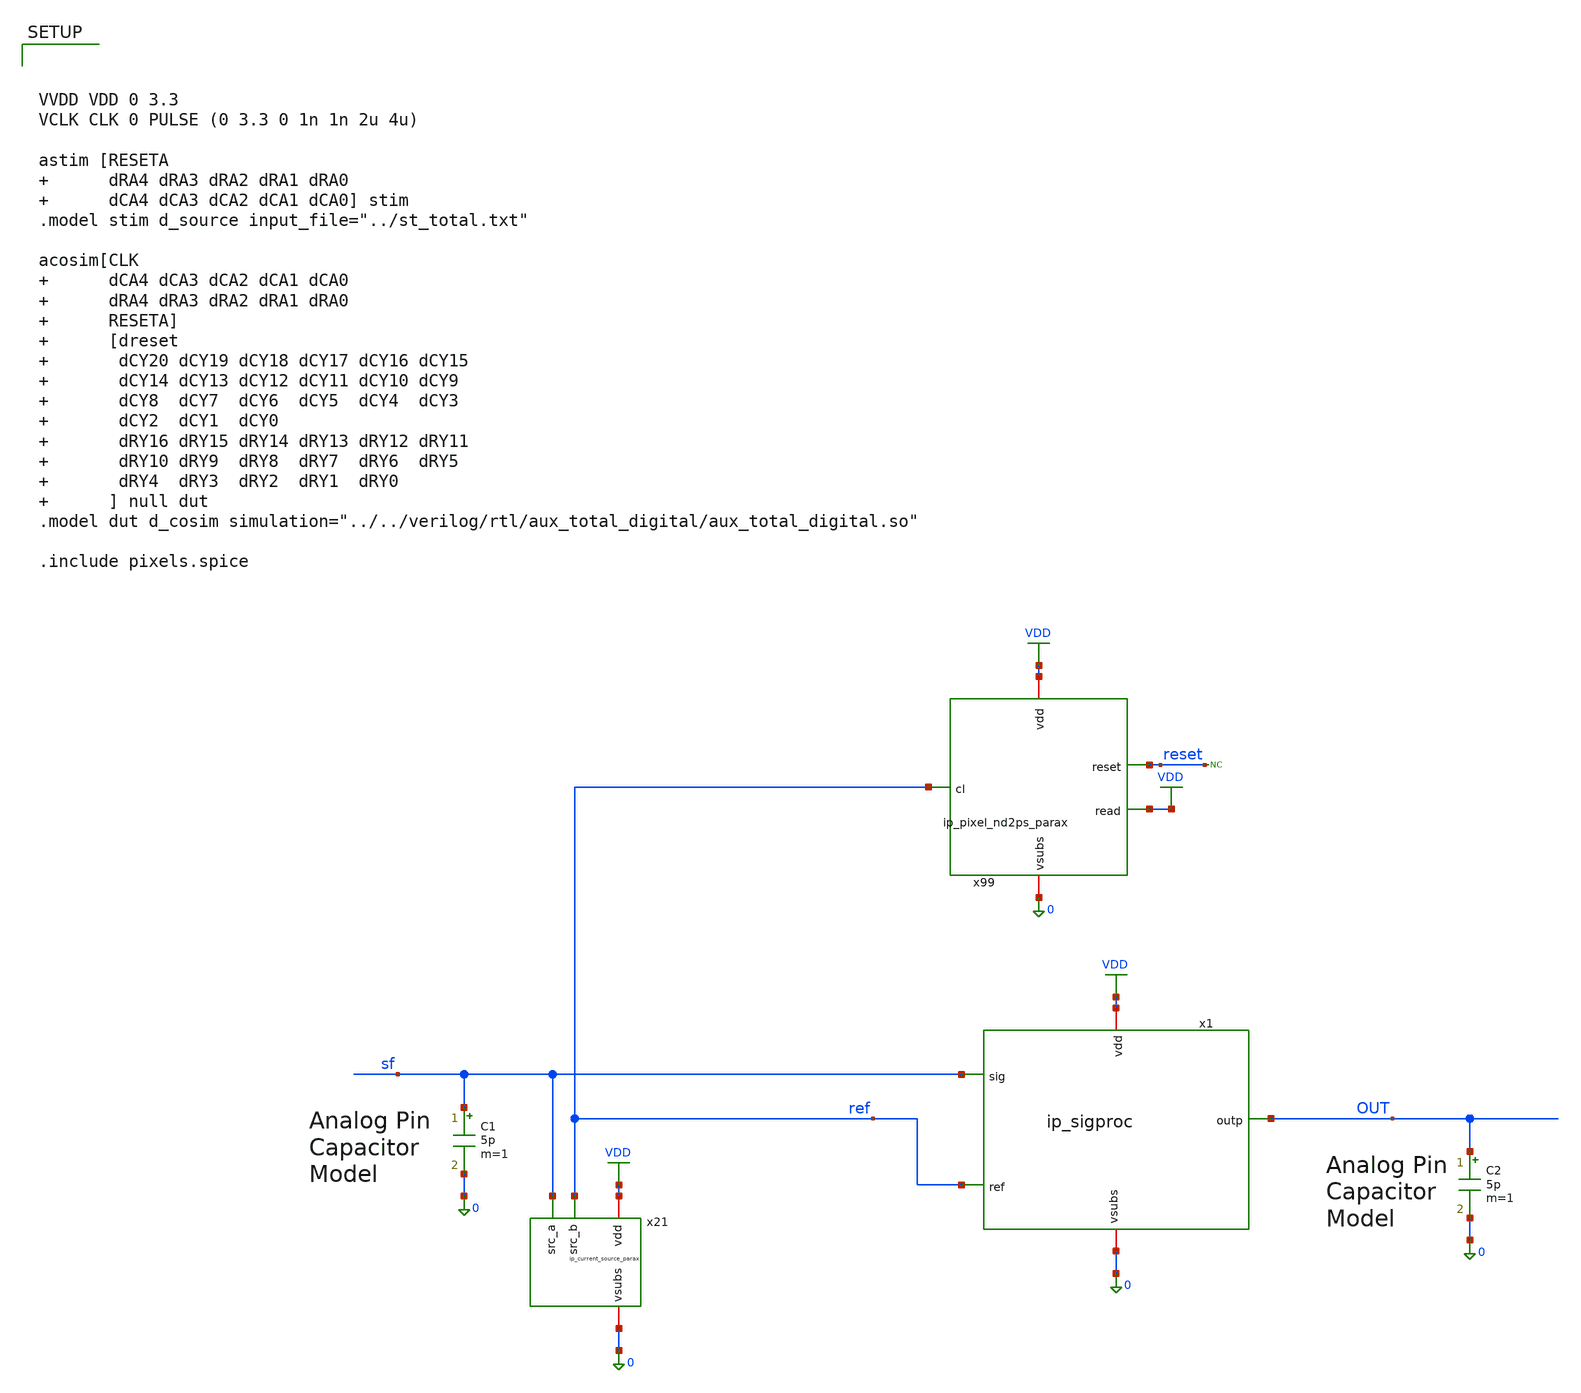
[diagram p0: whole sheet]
** sch_path: xschem/tb_total_tran.sch
**.subckt tb_total_tran
x21 VDD sf 0 ref ip_current_source_parax
x99 VDD reset VDD 0 ref ip_pixel_nd2ps_parax
C1 sf 0 5p m=1
C2 OUT 0 5p m=1
* noconn reset
x1 VDD OUT sf ref 0 ip_sigproc
**** begin user architecture code

.include $::180MCU_MODELS/design.ngspice
.lib $::180MCU_MODELS/sm141064.ngspice typical
.lib $::180MCU_MODELS/sm141064.ngspice res_typical
.lib $::180MCU_MODELS/sm141064.ngspice moscap_typical
.lib $::180MCU_MODELS/sm141064.ngspice diode_typical




.option klu
.option reltol=0.05
.option abstol=100u
.save none

.save V(nRA0) V(nRA1) V(nRA2) V(nRA3) V(nRA4)
.save V(nCA0) V(nCA1) V(nCA2) V(nCA3) V(nCA4)

.save V(ncy0) V(ncy1) V(ncy2) V(ncy3) V(ncy4) V(ncy5) V(ncy6) V(ncy7) V(ncy8)
.save V(ncy9) V(ncy10) V(ncy11) V(ncy12) V(ncy13) V(ncy14) V(ncy15) V(ncy16)
.save V(ncy17) V(ncy18) V(ncy19) V(ncy20)

.save V(nry0) V(nry1) V(nry2) V(nry3) V(nry4) V(nry5) V(nry6) V(nry7) V(nry8)
.save V(nry9) V(nry10) V(nry11) V(nry12) V(nry13) V(nry14) V(nry15) V(nry16)

.save V(reset) V(clk)
.save V(out) V(sf) V(ref) V(amp)
.control
	reset
	tran 100n 5.2m 0 100n
	write tb_total_tran.raw
	quit
.endc






VVDD VDD 0 3.3
VCLK CLK 0 PULSE (0 3.3 0 1n 1n 2u 4u)

astim [RESETA        dRA4 dRA3 dRA2 dRA1 dRA0        dCA4 dCA3 dCA2 dCA1 dCA0] stim
.model stim d_source input_file="../st_total.txt"

acosim[CLK        dCA4 dCA3 dCA2 dCA1 dCA0        dRA4 dRA3 dRA2 dRA1 dRA0        RESETA]
+        [dreset        dCY20 dCY19 dCY18 dCY17 dCY16 dCY15        dCY14 dCY13 dCY12 dCY11 dCY10 dCY9         dCY8
+  dCY7  dCY6  dCY5  dCY4  dCY3         dCY2  dCY1  dCY0         dRY16 dRY15 dRY14 dRY13 dRY12 dRY11
+         dRY10 dRY9  dRY8  dRY7  dRY6  dRY5        dRY4  dRY3  dRY2  dRY1  dRY0        ] null dut
.model dut d_cosim simulation="../../verilog/rtl/aux_total_digital/aux_total_digital.so"

.include pixels.spice


**** end user architecture code
**.ends

* expanding   symbol:  ip_current_source_parax.sym # of pins=4
** sym_path: xschem/ip_current_source.sym
.include [file normalize ./parax/ip_current_source.sim.spice]

* expanding   symbol:  ip_pixel_nd2ps_parax.sym # of pins=5
** sym_path: xschem/ip_pixel_nd2ps.sym
.include [file normalize ./parax/ip_pixel_nd2ps.sim.spice]

* expanding   symbol:  ip_sigproc.sym # of pins=5
** sym_path: xschem/ip_sigproc.sym
** sch_path: xschem/ip_sigproc.sch
.subckt ip_sigproc vdd outp sig ref vsubs
*.ipin sig
*.ipin ref
*.iopin vdd
*.iopin vsubs
*.opin outp
x1 vdd net1 sig net1 vsubs ip_amplifier
x2 vdd outp ref net2 net6 ip_amplifier
XR1 net1 net2 net7 ppolyf_u_1k r_width=1e-6 r_length=10e-6 m=1
XR2 net2 net3 net8 ppolyf_u_1k r_width=1e-6 r_length=10e-6 m=1
XR3 net3 net4 net9 ppolyf_u_1k r_width=1e-6 r_length=10e-6 m=1
XR4 net4 net5 net10 ppolyf_u_1k r_width=1e-6 r_length=10e-6 m=1
XR5 net5 outp net11 ppolyf_u_1k r_width=1e-6 r_length=10e-6 m=1
XC1 outp net2 cap_pmos_03v3 c_width=12e-6 c_length=12e-6 m=1
XC2 net2 outp cap_pmos_03v3 c_width=12e-6 c_length=12e-6 m=1
.ends


* expanding   symbol:  xschem/ip_amplifier.sym # of pins=5
** sym_path: xschem/ip_amplifier.sym
** sch_path: xschem/ip_amplifier.sch
.subckt ip_amplifier VDD OUTP INP INN VSUBS
*.iopin VDD
*.iopin VSUBS
*.ipin INP
*.ipin INN
*.opin OUTP
XM1 COMP INP COMMON_ VDD pfet_03v3 L=5u W=18.0u nf=1 ad='int((nf+1)/2) * W/nf * 0.18u' as='int((nf+2)/2) * W/nf * 0.18u'
+ pd='2*int((nf+1)/2) * (W/nf + 0.18u)' ps='2*int((nf+2)/2) * (W/nf + 0.18u)' nrd='0.18u / W' nrs='0.18u / W'
+ sa=0 sb=0 sd=0 m=1 par=1
XM2 net6 INN COMMON_ VDD pfet_03v3 L=5u W=18.0u nf=1 ad='int((nf+1)/2) * W/nf * 0.18u' as='int((nf+2)/2) * W/nf * 0.18u'
+ pd='2*int((nf+1)/2) * (W/nf + 0.18u)' ps='2*int((nf+2)/2) * (W/nf + 0.18u)' nrd='0.18u / W' nrs='0.18u / W'
+ sa=0 sb=0 sd=0 m=1 par=1
XM3 net2 NBIAS VSUBS vsubs nfet_03v3 L=2u W=6u nf=1 ad='int((nf+1)/2) * W/nf * 0.18u' as='int((nf+2)/2) * W/nf * 0.18u'
+ pd='2*int((nf+1)/2) * (W/nf + 0.18u)' ps='2*int((nf+2)/2) * (W/nf + 0.18u)' nrd='0.18u / W' nrs='0.18u / W'
+ sa=0 sb=0 sd=0 m=2 par=2
XM4 net1 NBIAS VSUBS vsubs nfet_03v3 L=2u W=6u nf=1 ad='int((nf+1)/2) * W/nf * 0.18u' as='int((nf+2)/2) * W/nf * 0.18u'
+ pd='2*int((nf+1)/2) * (W/nf + 0.18u)' ps='2*int((nf+2)/2) * (W/nf + 0.18u)' nrd='0.18u / W' nrs='0.18u / W'
+ sa=0 sb=0 sd=0 m=1 par=1
XM7 NBIAS NBIAS net2 vsubs nfet_03v3 L=0.5u W=6u nf=1 ad='int((nf+1)/2) * W/nf * 0.18u' as='int((nf+2)/2) * W/nf * 0.18u'
+ pd='2*int((nf+1)/2) * (W/nf + 0.18u)' ps='2*int((nf+2)/2) * (W/nf + 0.18u)' nrd='0.18u / W' nrs='0.18u / W'
+ sa=0 sb=0 sd=0 m=4 par=4
XM8 net3 NBIAS net1 vsubs nfet_03v3 L=0.5u W=6u nf=1 ad='int((nf+1)/2) * W/nf * 0.18u' as='int((nf+2)/2) * W/nf * 0.18u'
+ pd='2*int((nf+1)/2) * (W/nf + 0.18u)' ps='2*int((nf+2)/2) * (W/nf + 0.18u)' nrd='0.18u / W' nrs='0.18u / W'
+ sa=0 sb=0 sd=0 m=4 par=4
XM9 net4 PBIAS VDD VDD pfet_03v3 L=2u W=6u nf=1 ad='int((nf+1)/2) * W/nf * 0.18u' as='int((nf+2)/2) * W/nf * 0.18u'
+ pd='2*int((nf+1)/2) * (W/nf + 0.18u)' ps='2*int((nf+2)/2) * (W/nf + 0.18u)' nrd='0.18u / W' nrs='0.18u / W'
+ sa=0 sb=0 sd=0 m=1 par=1
XM10 net5 PBIAS VDD VDD pfet_03v3 L=2u W=6u nf=1 ad='int((nf+1)/2) * W/nf * 0.18u' as='int((nf+2)/2) * W/nf * 0.18u'
+ pd='2*int((nf+1)/2) * (W/nf + 0.18u)' ps='2*int((nf+2)/2) * (W/nf + 0.18u)' nrd='0.18u / W' nrs='0.18u / W'
+ sa=0 sb=0 sd=0 m=1 par=1
XM11 PBIAS PBIAS net4 VDD pfet_03v3 L=0.5u W=6u nf=1 ad='int((nf+1)/2) * W/nf * 0.18u' as='int((nf+2)/2) * W/nf * 0.18u'
+ pd='2*int((nf+1)/2) * (W/nf + 0.18u)' ps='2*int((nf+2)/2) * (W/nf + 0.18u)' nrd='0.18u / W' nrs='0.18u / W'
+ sa=0 sb=0 sd=0 m=4 par=4
XM12 COMMON PBIAS net5 VDD pfet_03v3 L=0.5u W=6u nf=1 ad='int((nf+1)/2) * W/nf * 0.18u' as='int((nf+2)/2) * W/nf * 0.18u'
+ pd='2*int((nf+1)/2) * (W/nf + 0.18u)' ps='2*int((nf+2)/2) * (W/nf + 0.18u)' nrd='0.18u / W' nrs='0.18u / W'
+ sa=0 sb=0 sd=0 m=4 par=4
XM13 COMP net6 VSUBS vsubs nfet_03v3 L=5u W=6u nf=1 ad='int((nf+1)/2) * W/nf * 0.18u' as='int((nf+2)/2) * W/nf * 0.18u'
+ pd='2*int((nf+1)/2) * (W/nf + 0.18u)' ps='2*int((nf+2)/2) * (W/nf + 0.18u)' nrd='0.18u / W' nrs='0.18u / W'
+ sa=0 sb=0 sd=0 m=1 par=1
XM14 net6 net6 VSUBS vsubs nfet_03v3 L=5u W=6u nf=1 ad='int((nf+1)/2) * W/nf * 0.18u' as='int((nf+2)/2) * W/nf * 0.18u'
+ pd='2*int((nf+1)/2) * (W/nf + 0.18u)' ps='2*int((nf+2)/2) * (W/nf + 0.18u)' nrd='0.18u / W' nrs='0.18u / W'
+ sa=0 sb=0 sd=0 m=1 par=1
XM17 net8 PBIAS VDD VDD pfet_03v3 L=0.5u W=12u nf=1 ad='int((nf+1)/2) * W/nf * 0.18u' as='int((nf+2)/2) * W/nf * 0.18u'
+ pd='2*int((nf+1)/2) * (W/nf + 0.18u)' ps='2*int((nf+2)/2) * (W/nf + 0.18u)' nrd='0.18u / W' nrs='0.18u / W'
+ sa=0 sb=0 sd=0 m=2 par=2
XM18 OUTP COMP VSUBS vsubs nfet_03v3 L=0.5u W=12u nf=1 ad='int((nf+1)/2) * W/nf * 0.18u' as='int((nf+2)/2) * W/nf * 0.18u'
+ pd='2*int((nf+1)/2) * (W/nf + 0.18u)' ps='2*int((nf+2)/2) * (W/nf + 0.18u)' nrd='0.18u / W' nrs='0.18u / W'
+ sa=0 sb=0 sd=0 m=4 par=4
XR3 NBIAS net7 vsubs ppolyf_u_1k r_width=1e-6 r_length=48e-6 m=1
Vmeas VDD net7 0
Vmeas1 PBIAS net3 0
XC1 OUTP net9 cap_pmos_03v3 c_width=13.5e-6 c_length=18e-6 m=1
XC2 COMP net9 cap_pmos_03v3 c_width=13.5e-6 c_length=18e-6 m=1
Vmeas2 COMMON COMMON_ 0
Vmeas3 net8 OUTP 0
XR2 VDD net9 vsubs ppolyf_u_1k r_width=1e-6 r_length=96e-6 m=1
.ends

.GLOBAL VDD
.end
